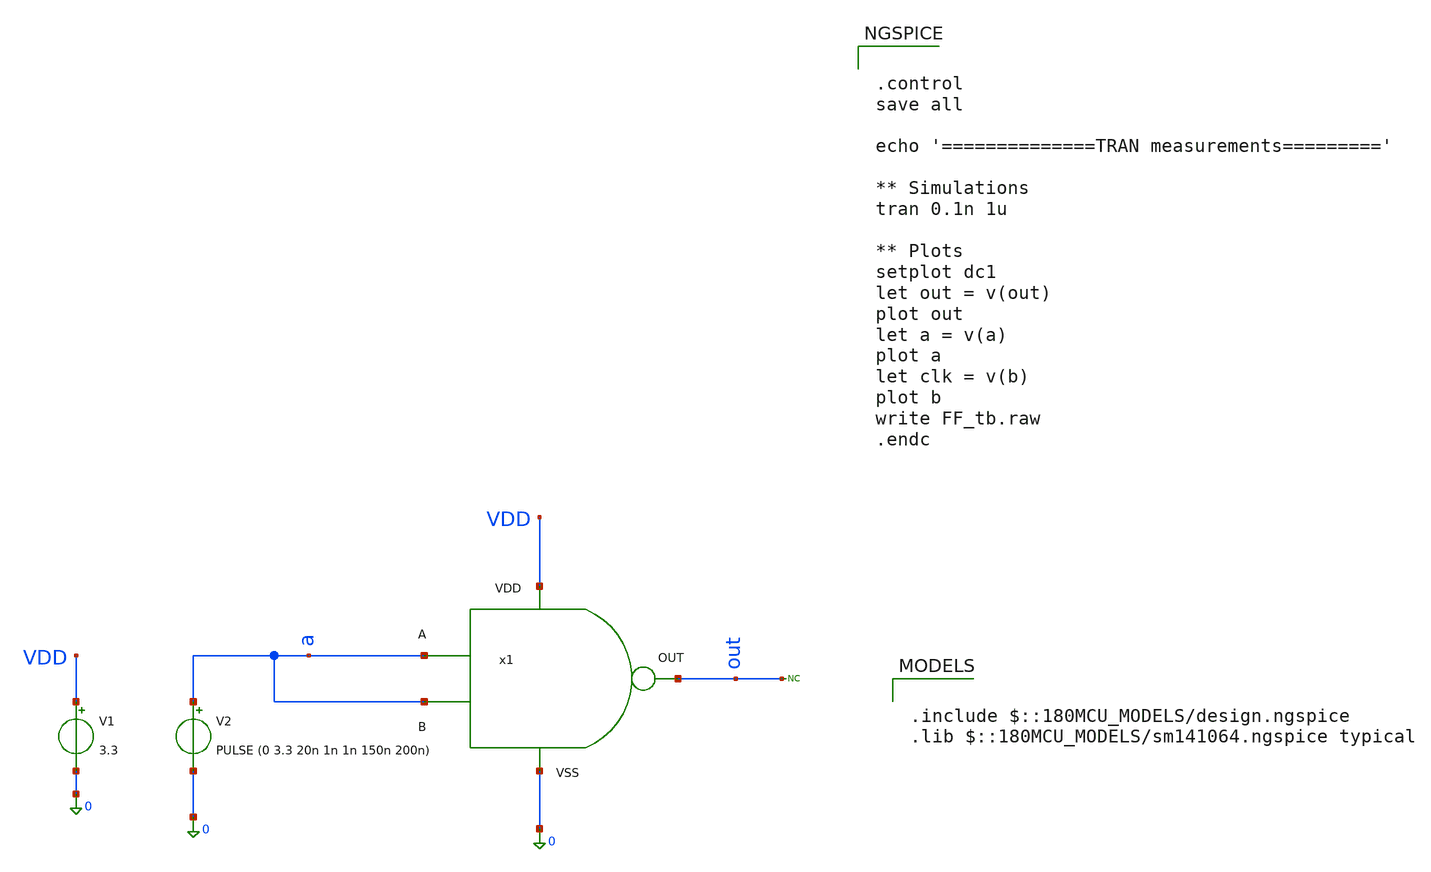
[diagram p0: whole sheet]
** sch_path: designs/sar_adc/digital/gate_nand_x1/xschem/NAND_tb.sch
**.subckt NAND_tb
x1 VDD 0 a a out NAND
V1 VDD 0 3.3
V2 a 0 PULSE (0 3.3 20n 1n 1n 150n 200n)
* noconn out
**** begin user architecture code


.control
save all

echo '==============TRAN measurements========='

** Simulations
tran 0.1n 1u

** Plots
setplot dc1
let out = v(out)
plot out
let a = v(a)
plot a
let clk = v(b)
plot b
write FF_tb.raw
.endc



.include $::180MCU_MODELS/design.ngspice
.lib $::180MCU_MODELS/sm141064.ngspice typical

**** end user architecture code
**.ends

* expanding   symbol:  sar_adc/digital/NAND/xschem/NAND.sym # of pins=5
** sym_path: designs/sar_adc/digital/NAND/xschem/NAND.sym
** sch_path: designs/sar_adc/digital/NAND/xschem/NAND.sch
.subckt NAND VDD VSS A B out
*.iopin VDD
*.iopin A
*.iopin B
*.iopin out
*.iopin VSS
xINVA VDD net1 net2 VSS inverter
xINVB[2] VDD net2 out VSS inverter
xINVB[1] VDD net2 out VSS inverter
xINVB[0] VDD net2 out VSS inverter
XM2 net1 A VDD VDD pfet_03v3 L=0.28u W=0.5u nf=1 ad='int((nf+1)/2) * W/nf * 0.18u' as='int((nf+2)/2) * W/nf * 0.18u'
+ pd='2*int((nf+1)/2) * (W/nf + 0.18u)' ps='2*int((nf+2)/2) * (W/nf + 0.18u)' nrd='0.18u / W' nrs='0.18u / W'
+ sa=0 sb=0 sd=0 m=2
XM1 net1 A net3 VSS nfet_03v3 L=0.28u W=0.5u nf=1 ad='int((nf+1)/2) * W/nf * 0.18u' as='int((nf+2)/2) * W/nf * 0.18u'
+ pd='2*int((nf+1)/2) * (W/nf + 0.18u)' ps='2*int((nf+2)/2) * (W/nf + 0.18u)' nrd='0.18u / W' nrs='0.18u / W'
+ sa=0 sb=0 sd=0 m=1
XM3 net1 B VDD VDD pfet_03v3 L=0.28u W=0.5u nf=1 ad='int((nf+1)/2) * W/nf * 0.18u' as='int((nf+2)/2) * W/nf * 0.18u'
+ pd='2*int((nf+1)/2) * (W/nf + 0.18u)' ps='2*int((nf+2)/2) * (W/nf + 0.18u)' nrd='0.18u / W' nrs='0.18u / W'
+ sa=0 sb=0 sd=0 m=2
XM4 net3 B VSS VSS nfet_03v3 L=0.28u W=0.5u nf=1 ad='int((nf+1)/2) * W/nf * 0.18u' as='int((nf+2)/2) * W/nf * 0.18u'
+ pd='2*int((nf+1)/2) * (W/nf + 0.18u)' ps='2*int((nf+2)/2) * (W/nf + 0.18u)' nrd='0.18u / W' nrs='0.18u / W'
+ sa=0 sb=0 sd=0 m=1
.ends


* expanding   symbol:  designs/sar_adc/digital/inverter/xschem/inverter.sym # of pins=6
** sym_path: designs/sar_adc/digital/inverter/xschem/inverter.sym
** sch_path: designs/sar_adc/digital/inverter/xschem/inverter.sch
.subckt inverter VDD in out VSS
*.opin out
*.iopin in
*.iopin VDD
*.iopin VSS
XM1 out in VSS VSS nfet_03v3 L=0.28u W=1u nf=1 ad='int((nf+1)/2) * W/nf * 0.18u' as='int((nf+2)/2) * W/nf * 0.18u'
+ pd='2*int((nf+1)/2) * (W/nf + 0.18u)' ps='2*int((nf+2)/2) * (W/nf + 0.18u)' nrd='0.18u / W' nrs='0.18u / W'
+ sa=0 sb=0 sd=0 m=1
XM2 out in VDD VDD pfet_03v3 L=0.28u W=3u nf=1 ad='int((nf+1)/2) * W/nf * 0.18u' as='int((nf+2)/2) * W/nf * 0.18u'
+ pd='2*int((nf+1)/2) * (W/nf + 0.18u)' ps='2*int((nf+2)/2) * (W/nf + 0.18u)' nrd='0.18u / W' nrs='0.18u / W'
+ sa=0 sb=0 sd=0 m=1
.ends

.end
